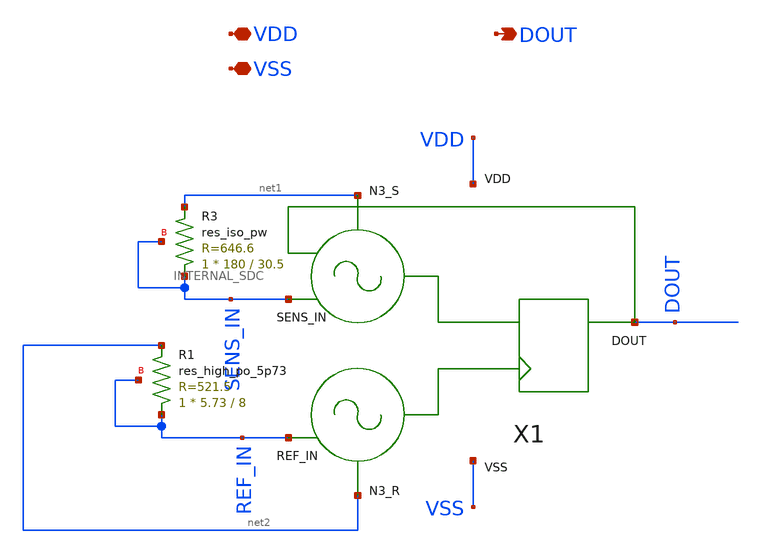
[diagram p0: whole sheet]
** sch_path: samples/cace-tests/SDC/xschem/SDC.sch
**.subckt SDC VDD VSS DOUT
*.iopin VDD
*.iopin VSS
*.opin DOUT
X1 SENS_IN REF_IN DOUT VDD VSS net1 net2 INTERNAL_SDC
XR1 REF_IN net2 REF_IN sky130_fd_pr__res_high_po_5p73 L=8 mult=1 m=1
XR3 SENS_IN net1 SENS_IN sky130_fd_pr__res_iso_pw W=180 L=30.5 m=1
**.ends

* expanding   symbol:  INTERNAL_SDC.sym # of pins=7
** sym_path: samples/cace-tests/SDC/xschem/INTERNAL_SDC.sym
** sch_path: samples/cace-tests/SDC/xschem/INTERNAL_SDC.sch
.subckt INTERNAL_SDC SENS_IN REF_IN DOUT VDD VSS N3_S N3_R
*.iopin VDD
*.iopin VSS
*.ipin SENS_IN
*.ipin REF_IN
*.opin DOUT
*.ipin N3_S
*.ipin N3_R
XOSC_SENS SENS_IN N1_S N2_S VDD VSS net1 N3_S OSC_v7p1
XOSC_REF REF_IN N1_R N2_R VDD VSS net2 N3_R OSC_v7p1
XPG SENS_IN DOUT net1 VDD VSS PASSGATE_v1p2
XPG1 REF_IN VDD net2 VDD VSS PASSGATE_v1p2
X1 N2_S N2_R DOUT nDOUT VDD VSS DFF_v4p1
.ends


* expanding   symbol:  OSC_v7p1.sym # of pins=7
** sym_path: samples/cace-tests/SDC/xschem/OSC_v7p1.sym
** sch_path: samples/cace-tests/SDC/xschem/OSC_v7p1.sch
.subckt OSC_v7p1 SENS_IN N1 N2 VDD VSS CON_CV N3
*.ipin SENS_IN
*.iopin VDD
*.iopin VSS
*.opin N1
*.opin N2
*.iopin CON_CV
*.opin N3
XST1 SENS_IN VDD VSS N1 N1 N1 INVandCAP_v4p1
XST2 N1 VDD VSS net1 net1 net1 INVandCAP_v4p1
XST3 net1 VDD VSS N3 CON_CV SENS_IN INVandCAP_v4p1
XBUFFS net1 N2 VDD VSS BUFFMIN_v1p1
.ends


* expanding   symbol:  PASSGATE_v1p2.sym # of pins=5
** sym_path: samples/cace-tests/SDC/xschem/PASSGATE_v1p2.sym
** sch_path: samples/cace-tests/SDC/xschem/PASSGATE_v1p2.sch
.subckt PASSGATE_v1p2 VIN CTR VOUT VDD VSS
*.ipin VIN
*.iopin VDD
*.iopin VSS
*.ipin CTR
*.opin VOUT
XMNSW VOUT CTR VIN VSS sky130_fd_pr__nfet_01v8 L=0.15 W=2 nf=1 ad='int((nf+1)/2) * W/nf * 0.29' as='int((nf+2)/2) * W/nf * 0.29'
+ pd='2*int((nf+1)/2) * (W/nf + 0.29)' ps='2*int((nf+2)/2) * (W/nf + 0.29)' nrd='0.29 / W' nrs='0.29 / W'
+ sa=0 sb=0 sd=0 mult=1 m=1
XMPSW VOUT net1 VIN VDD sky130_fd_pr__pfet_01v8 L=0.15 W=6 nf=1 ad='int((nf+1)/2) * W/nf * 0.29' as='int((nf+2)/2) * W/nf * 0.29'
+ pd='2*int((nf+1)/2) * (W/nf + 0.29)' ps='2*int((nf+2)/2) * (W/nf + 0.29)' nrd='0.29 / W' nrs='0.29 / W'
+ sa=0 sb=0 sd=0 mult=1 m=1
X1 CTR net1 VDD VSS INVMIN_v1p1
.ends


* expanding   symbol:  DFF_v4p1.sym # of pins=6
** sym_path: samples/cace-tests/SDC/xschem/DFF_v4p1.sym
** sch_path: samples/cace-tests/SDC/xschem/DFF_v4p1.sch
.subckt DFF_v4p1 IN CLK D ND VDD GND
*.ipin IN
*.ipin CLK
*.iopin VDD
*.iopin GND
*.opin ND
*.opin D
XMN_NIN NDIFF IN GND GND sky130_fd_pr__nfet_01v8 L=0.15 W=1 nf=1 ad='int((nf+1)/2) * W/nf * 0.29' as='int((nf+2)/2) * W/nf * 0.29'
+ pd='2*int((nf+1)/2) * (W/nf + 0.29)' ps='2*int((nf+2)/2) * (W/nf + 0.29)' nrd='0.29 / W' nrs='0.29 / W'
+ sa=0 sb=0 sd=0 mult=1 m=1
XMP_NINCLK NDIFF CLK net1 VDD sky130_fd_pr__pfet_01v8 L=0.15 W=1 nf=1 ad='int((nf+1)/2) * W/nf * 0.29'
+ as='int((nf+2)/2) * W/nf * 0.29' pd='2*int((nf+1)/2) * (W/nf + 0.29)' ps='2*int((nf+2)/2) * (W/nf + 0.29)'
+ nrd='0.29 / W' nrs='0.29 / W' sa=0 sb=0 sd=0 mult=1 m=1
XMP_NIN net1 IN VDD VDD sky130_fd_pr__pfet_01v8 L=0.15 W=1 nf=1 ad='int((nf+1)/2) * W/nf * 0.29' as='int((nf+2)/2) * W/nf * 0.29'
+ pd='2*int((nf+1)/2) * (W/nf + 0.29)' ps='2*int((nf+2)/2) * (W/nf + 0.29)' nrd='0.29 / W' nrs='0.29 / W'
+ sa=0 sb=0 sd=0 mult=1 m=1
XMN_NIN1 PDIFF NDIFF GND GND sky130_fd_pr__nfet_01v8 L=0.15 W=1 nf=1 ad='int((nf+1)/2) * W/nf * 0.29'
+ as='int((nf+2)/2) * W/nf * 0.29' pd='2*int((nf+1)/2) * (W/nf + 0.29)' ps='2*int((nf+2)/2) * (W/nf + 0.29)'
+ nrd='0.29 / W' nrs='0.29 / W' sa=0 sb=0 sd=0 mult=1 m=1
XMP_NINCLK1 PDIFF CLK net2 VDD sky130_fd_pr__pfet_01v8 L=0.15 W=1 nf=1 ad='int((nf+1)/2) * W/nf * 0.29'
+ as='int((nf+2)/2) * W/nf * 0.29' pd='2*int((nf+1)/2) * (W/nf + 0.29)' ps='2*int((nf+2)/2) * (W/nf + 0.29)'
+ nrd='0.29 / W' nrs='0.29 / W' sa=0 sb=0 sd=0 mult=1 m=1
XMP_NIN1 net2 NDIFF VDD VDD sky130_fd_pr__pfet_01v8 L=0.15 W=1 nf=1 ad='int((nf+1)/2) * W/nf * 0.29'
+ as='int((nf+2)/2) * W/nf * 0.29' pd='2*int((nf+1)/2) * (W/nf + 0.29)' ps='2*int((nf+2)/2) * (W/nf + 0.29)'
+ nrd='0.29 / W' nrs='0.29 / W' sa=0 sb=0 sd=0 mult=1 m=1
XMN_NIN2 net3 CLK GND GND sky130_fd_pr__nfet_01v8 L=0.15 W=1 nf=1 ad='int((nf+1)/2) * W/nf * 0.29' as='int((nf+2)/2) * W/nf * 0.29'
+ pd='2*int((nf+1)/2) * (W/nf + 0.29)' ps='2*int((nf+2)/2) * (W/nf + 0.29)' nrd='0.29 / W' nrs='0.29 / W'
+ sa=0 sb=0 sd=0 mult=1 m=1
XMN_POUTT ND PDIFF net3 GND sky130_fd_pr__nfet_01v8 L=0.15 W=1 nf=1 ad='int((nf+1)/2) * W/nf * 0.29'
+ as='int((nf+2)/2) * W/nf * 0.29' pd='2*int((nf+1)/2) * (W/nf + 0.29)' ps='2*int((nf+2)/2) * (W/nf + 0.29)'
+ nrd='0.29 / W' nrs='0.29 / W' sa=0 sb=0 sd=0 mult=1 m=1
XMN_POUTT1 D NDIFF net4 GND sky130_fd_pr__nfet_01v8 L=0.15 W=1 nf=1 ad='int((nf+1)/2) * W/nf * 0.29'
+ as='int((nf+2)/2) * W/nf * 0.29' pd='2*int((nf+1)/2) * (W/nf + 0.29)' ps='2*int((nf+2)/2) * (W/nf + 0.29)'
+ nrd='0.29 / W' nrs='0.29 / W' sa=0 sb=0 sd=0 mult=1 m=1
XMN_POUTT2 D ND GND GND sky130_fd_pr__nfet_01v8 L=0.15 W=1 nf=1 ad='int((nf+1)/2) * W/nf * 0.29' as='int((nf+2)/2) * W/nf * 0.29'
+ pd='2*int((nf+1)/2) * (W/nf + 0.29)' ps='2*int((nf+2)/2) * (W/nf + 0.29)' nrd='0.29 / W' nrs='0.29 / W'
+ sa=0 sb=0 sd=0 mult=1 m=1
XMP_NIN2 D ND VDD VDD sky130_fd_pr__pfet_01v8 L=0.15 W=1 nf=1 ad='int((nf+1)/2) * W/nf * 0.29' as='int((nf+2)/2) * W/nf * 0.29'
+ pd='2*int((nf+1)/2) * (W/nf + 0.29)' ps='2*int((nf+2)/2) * (W/nf + 0.29)' nrd='0.29 / W' nrs='0.29 / W'
+ sa=0 sb=0 sd=0 mult=1 m=1
XMN_POUTT3 ND D GND GND sky130_fd_pr__nfet_01v8 L=0.15 W=1 nf=1 ad='int((nf+1)/2) * W/nf * 0.29' as='int((nf+2)/2) * W/nf * 0.29'
+ pd='2*int((nf+1)/2) * (W/nf + 0.29)' ps='2*int((nf+2)/2) * (W/nf + 0.29)' nrd='0.29 / W' nrs='0.29 / W'
+ sa=0 sb=0 sd=0 mult=1 m=1
XMP_NIN3 ND D VDD VDD sky130_fd_pr__pfet_01v8 L=0.15 W=1 nf=1 ad='int((nf+1)/2) * W/nf * 0.29' as='int((nf+2)/2) * W/nf * 0.29'
+ pd='2*int((nf+1)/2) * (W/nf + 0.29)' ps='2*int((nf+2)/2) * (W/nf + 0.29)' nrd='0.29 / W' nrs='0.29 / W'
+ sa=0 sb=0 sd=0 mult=1 m=1
XMN_NIN3 net4 CLK GND GND sky130_fd_pr__nfet_01v8 L=0.15 W=1 nf=1 ad='int((nf+1)/2) * W/nf * 0.29' as='int((nf+2)/2) * W/nf * 0.29'
+ pd='2*int((nf+1)/2) * (W/nf + 0.29)' ps='2*int((nf+2)/2) * (W/nf + 0.29)' nrd='0.29 / W' nrs='0.29 / W'
+ sa=0 sb=0 sd=0 mult=1 m=1
.ends


* expanding   symbol:  INVandCAP_v4p1.sym # of pins=6
** sym_path: samples/cace-tests/SDC/xschem/INVandCAP_v4p1.sym
** sch_path: samples/cace-tests/SDC/xschem/INVandCAP_v4p1.sch
.subckt INVandCAP_v4p1 VIN VDD VSS VOUT CON_CV CON_CBASE
*.ipin VIN
*.iopin VDD
*.iopin VSS
*.opin VOUT
*.iopin CON_CV
*.iopin CON_CBASE
XINV_OSC VIN VOUT VDD VSS INV_v1p1
XCN CON_CV CON_CBASE VSS CAPOSC_v3p1
.ends


* expanding   symbol:  BUFFMIN_v1p1.sym # of pins=4
** sym_path: samples/cace-tests/SDC/xschem/BUFFMIN_v1p1.sym
** sch_path: samples/cace-tests/SDC/xschem/BUFFMIN_v1p1.sch
.subckt BUFFMIN_v1p1 VIN VOUT VDD VSS
*.iopin VDD
*.iopin VSS
*.ipin VIN
*.opin VOUT
X1 VIN net1 VDD VSS INVMIN_v1p1
X2 net1 VOUT VDD VSS INVMIN_v1p1
.ends


* expanding   symbol:  INVMIN_v1p1.sym # of pins=4
** sym_path: samples/cace-tests/SDC/xschem/INVMIN_v1p1.sym
** sch_path: samples/cace-tests/SDC/xschem/INVMIN_v1p1.sch
.subckt INVMIN_v1p1 VIN VOUT VDD VSS
*.ipin VIN
*.iopin VDD
*.iopin VSS
*.opin VOUT
XM1 VOUT VIN VSS VSS sky130_fd_pr__nfet_01v8 L=0.15 W=1 nf=1 ad='int((nf+1)/2) * W/nf * 0.29' as='int((nf+2)/2) * W/nf * 0.29'
+ pd='2*int((nf+1)/2) * (W/nf + 0.29)' ps='2*int((nf+2)/2) * (W/nf + 0.29)' nrd='0.29 / W' nrs='0.29 / W'
+ sa=0 sb=0 sd=0 mult=1 m=1
XM2 VOUT VIN VDD VDD sky130_fd_pr__pfet_01v8 L=0.15 W=1 nf=1 ad='int((nf+1)/2) * W/nf * 0.29' as='int((nf+2)/2) * W/nf * 0.29'
+ pd='2*int((nf+1)/2) * (W/nf + 0.29)' ps='2*int((nf+2)/2) * (W/nf + 0.29)' nrd='0.29 / W' nrs='0.29 / W'
+ sa=0 sb=0 sd=0 mult=1 m=1
.ends


* expanding   symbol:  INV_v1p1.sym # of pins=4
** sym_path: samples/cace-tests/SDC/xschem/INV_v1p1.sym
** sch_path: samples/cace-tests/SDC/xschem/INV_v1p1.sch
.subckt INV_v1p1 VIN VOUT VDD VSS
*.ipin VIN
*.iopin VDD
*.iopin VSS
*.opin VOUT
XM1 VOUT VIN VSS VSS sky130_fd_pr__nfet_01v8 L=0.15 W=2 nf=2 ad='int((nf+1)/2) * W/nf * 0.29' as='int((nf+2)/2) * W/nf * 0.29'
+ pd='2*int((nf+1)/2) * (W/nf + 0.29)' ps='2*int((nf+2)/2) * (W/nf + 0.29)' nrd='0.29 / W' nrs='0.29 / W'
+ sa=0 sb=0 sd=0 mult=1 m=1
XM2 VOUT VIN VDD VDD sky130_fd_pr__pfet_01v8 L=0.15 W=6 nf=6 ad='int((nf+1)/2) * W/nf * 0.29' as='int((nf+2)/2) * W/nf * 0.29'
+ pd='2*int((nf+1)/2) * (W/nf + 0.29)' ps='2*int((nf+2)/2) * (W/nf + 0.29)' nrd='0.29 / W' nrs='0.29 / W'
+ sa=0 sb=0 sd=0 mult=1 m=1
.ends


* expanding   symbol:  CAPOSC_v3p1.sym # of pins=3
** sym_path: samples/cace-tests/SDC/xschem/CAPOSC_v3p1.sym
** sch_path: samples/cace-tests/SDC/xschem/CAPOSC_v3p1.sch
.subckt CAPOSC_v3p1 TOP_V TOP_B BOT
*.iopin TOP_V
*.iopin TOP_B
*.iopin BOT
XC1_V TOP_V BOT sky130_fd_pr__cap_mim_m3_1 W=10 L=10 MF=1 m=1
XC2_V TOP_V BOT sky130_fd_pr__cap_mim_m3_2 W=10 L=10 MF=1 m=1
XC1_B TOP_B BOT sky130_fd_pr__cap_mim_m3_1 W=10 L=10 MF=1 m=1
XC2_B TOP_B BOT sky130_fd_pr__cap_mim_m3_2 W=10 L=10 MF=1 m=1
XC5_B TOP_B BOT sky130_fd_pr__cap_mim_m3_1 W=10 L=10 MF=1 m=1
XC6_B TOP_B BOT sky130_fd_pr__cap_mim_m3_2 W=10 L=10 MF=1 m=1
XC3_B TOP_B BOT sky130_fd_pr__cap_mim_m3_1 W=10 L=10 MF=1 m=1
XC4_B TOP_B BOT sky130_fd_pr__cap_mim_m3_2 W=10 L=10 MF=1 m=1
XC7_B TOP_B BOT sky130_fd_pr__cap_mim_m3_1 W=10 L=10 MF=1 m=1
XC8_B TOP_B BOT sky130_fd_pr__cap_mim_m3_2 W=10 L=10 MF=1 m=1
XC9_B TOP_B BOT sky130_fd_pr__cap_mim_m3_1 W=10 L=10 MF=1 m=1
XC10_B TOP_B BOT sky130_fd_pr__cap_mim_m3_2 W=10 L=10 MF=1 m=1
.ends

.end
